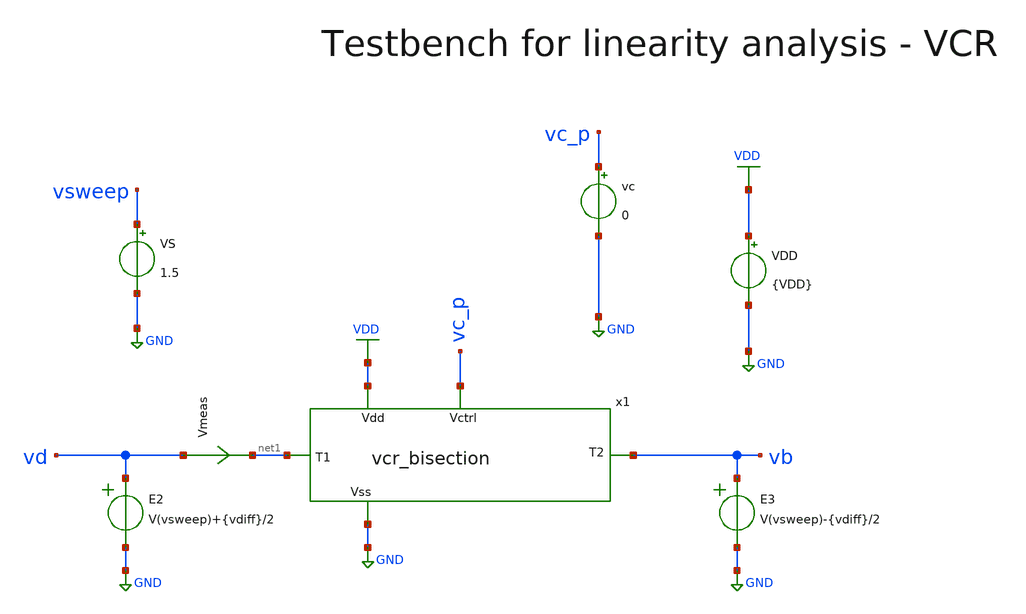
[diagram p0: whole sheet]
** sch_path: macros/voltage_controlled_resistors/macros/vcr_bisection/testbenches/xschem/res_tb_linearity_vcm.sch
**.subckt res_tb_linearity_vcm
VDD VDD GND {VDD}
VS vsweep GND 1.5
Vmeas vd net1 0
.save i(vmeas)
E2 vd GND VOL=' V(vsweep)+{vdiff}/2 '
E3 vb GND VOL=' V(vsweep)-{vdiff}/2 '
vc vc_p GND 0
x1 vc_p net1 vb VDD GND vcr_bisection
**** begin user architecture code

.lib cornerMOSlv.lib mos_tt
.lib cornerMOShv.lib mos_tt
.lib cornerRES.lib res_typ
.lib cornerDIO.lib dio_tt
.lib cornerCAP.lib cap_typ



* .include ../../../netlist/pex/inverter_magic_pex_3.spice
.param VDD=3.3
.csparam VDD=VDD
.param temp=27
.param vdiff=10m
.options savecurrents klu method=gear reltol=1e-3 abstol=1e-15 gmin=1e-15 rshunt=1e13
.control
let vcc = 1

save all
set appendwrite



repeat 10
  alter vc $&vcc

  * DC Sweep
  dc VS 0 3.3 10m
  remzerovec
  let vcc = vcc + 0.25
end
write @schname\.raw
set appendwrite

* Plotting
plot (dc1.v(vd) - dc1.v(vb))/(dc1.i(vmeas)) (dc2.v(vd) - dc2.v(vb))/(dc2.i(vmeas)) (dc3.v(vd) -
+ dc3.v(vb))/(dc3.i(vmeas)) (dc4.v(vd) - dc4.v(vb))/(dc4.i(vmeas)) (dc5.v(vd) - dc5.v(vb))/(dc5.i(vmeas)) ylimit 0 10k

plot dc1.i(vmeas) dc2.i(vmeas) dc3.i(vmeas) dc4.i(vmeas) dc5.i(vmeas)

* Write Data
unset appendwrite
set wr_vecnames
set wr_singlescale
wrdata ../plot_simulations/data/@schname\.txt v(vc_p) dc1.v(vsweep)/(dc1.i(Vmeas))
+ dc2.v(vsweep)/(dc2.i(Vmeas)) dc3.v(vsweep)/(dc3.i(Vmeas)) dc4.v(vsweep)/(dc4.i(Vmeas)) dc5.v(vsweep)/(dc5.i(Vmeas))

write res_tb_linearity.raw

*quit
.endc


**** end user architecture code
**.ends
.GLOBAL GND
.GLOBAL VDD
.end
